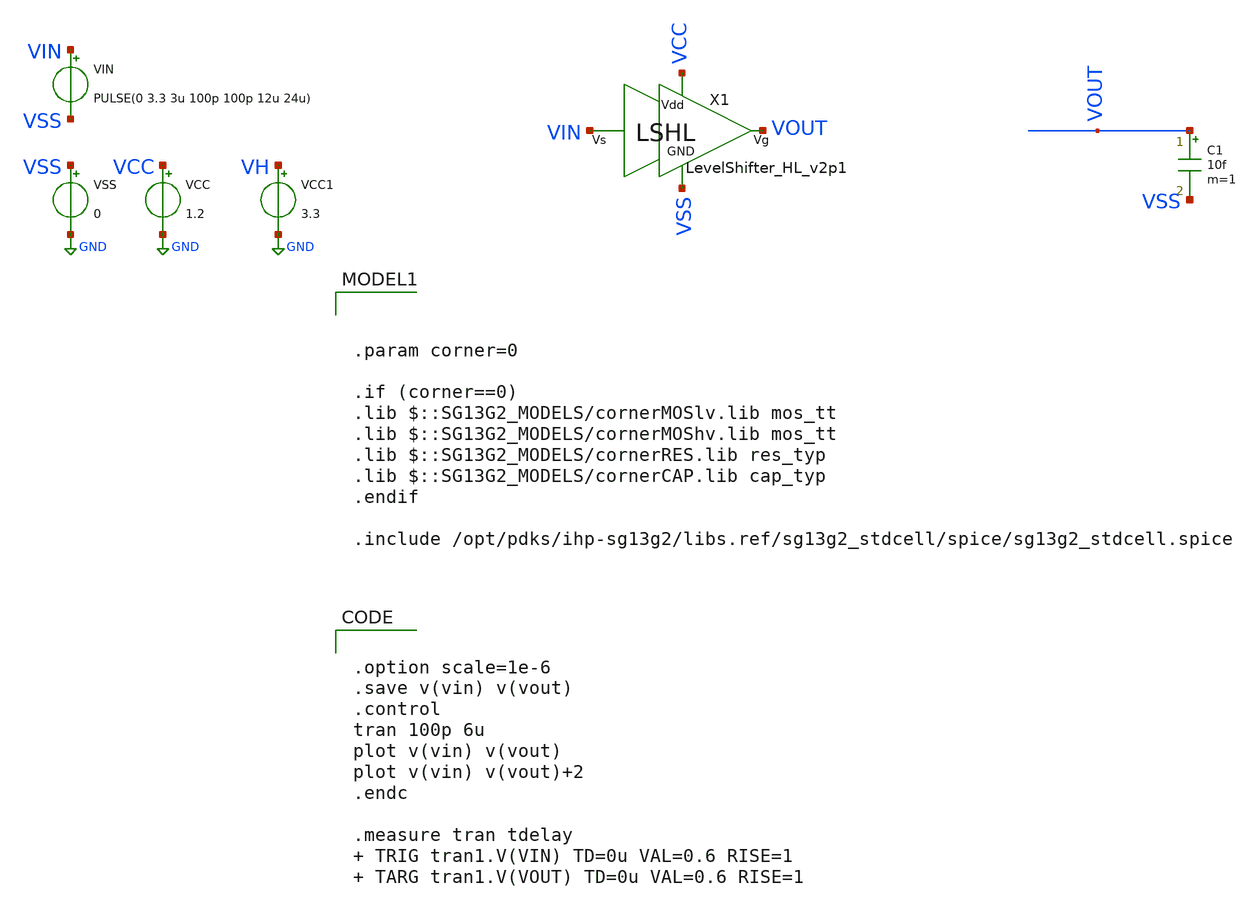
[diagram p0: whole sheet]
** sch_path: xschem/tb_LSHL_v2p1.sch
**.subckt tb_LSHL_v2p1
VCC VCC GND 1.2
VSS VSS GND 0
VIN VIN VSS PULSE(0 3.3 3u 100p 100p 12u 24u)
C1 VOUT VSS 10f m=1
X1 VIN VOUT VCC VSS LevelShifter_HL_v2p1
VCC1 VH GND 3.3
**** begin user architecture code


.option scale=1e-6
.save v(vin) v(vout)
.control
tran 100p 6u
plot v(vin) v(vout)
plot v(vin) v(vout)+2
.endc

.measure tran tdelay  TRIG tran1.V(VIN) TD=0u VAL=0.6 RISE=1  TARG tran1.V(VOUT) TD=0u VAL=0.6
+ RISE=1






.param corner=0

.if (corner==0)
.lib $::SG13G2_MODELS/cornerMOSlv.lib mos_tt
.lib $::SG13G2_MODELS/cornerMOShv.lib mos_tt
.lib $::SG13G2_MODELS/cornerRES.lib res_typ
.lib $::SG13G2_MODELS/cornerCAP.lib cap_typ
.endif

.include /opt/pdks/ihp-sg13g2/libs.ref/sg13g2_stdcell/spice/sg13g2_stdcell.spice

**** end user architecture code
**.ends

* expanding   symbol:  /home/designer/shared/TO202410_IHP_TDBuck/xschem/LevelShifter_HL_v2p1.sym #
*+ of pins=4
** sym_path: xschem/LevelShifter_HL_v2p1.sym
** sch_path: xschem/LevelShifter_HL_v2p1.sch
.subckt LevelShifter_HL_v2p1 Vs Vg Vdd GND
*.iopin Vdd
*.ipin Vs
*.opin Vg
*.iopin GND
XMD9 Vg VgMD2 Vdd Vdd sg13_lv_pmos w=1u l=0.13u ng=1 m=2 mm_ok=1
XMD5 VgMD2 Vs Vdd Vdd sg13_hv_pmos w=1u l=0.4u ng=1 m=2 mm_ok=1
XMD6 GND Vs VgMD2 GND sg13_hv_nmos w=1u l=0.45u ng=1 m=1 mm_ok=1
XMD2 GND VgMD2 Vg GND sg13_lv_nmos w=1u l=0.13u ng=1 m=1 mm_ok=1
.ends

.GLOBAL GND
.end
